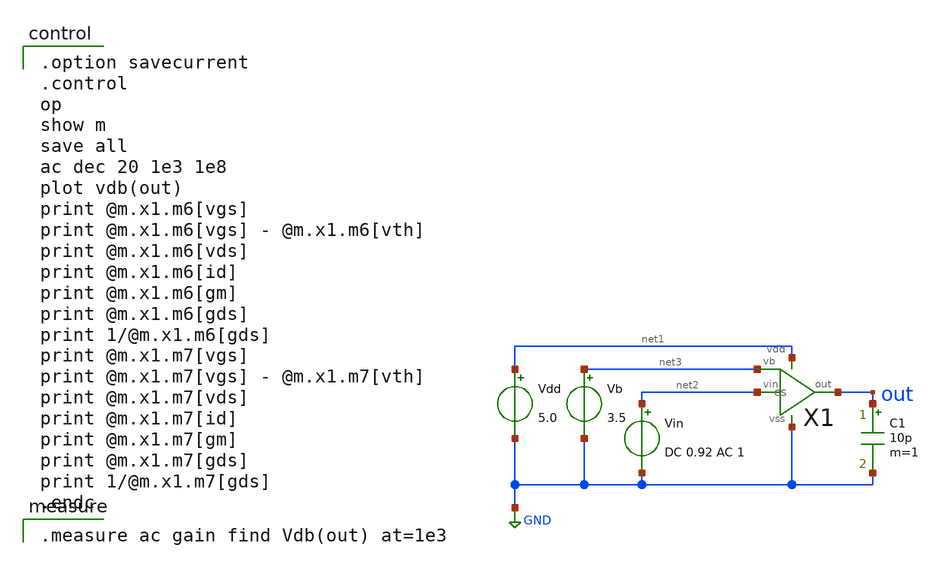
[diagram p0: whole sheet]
** sch_path: OR1/PTC06/opamp/cs_ac.sch
**.subckt cs_ac
Vdd net1 GND 5.0
Vb net3 GND 3.5
Vin net2 GND DC 0.92 AC 1
X1 net2 net3 out net1 GND cs
C1 out GND 10p m=1
**** begin user architecture code

.option savecurrent
.control
op
show m
save all
ac dec 20 1e3 1e8
plot vdb(out)
print @m.x1.m6[vgs]
print @m.x1.m6[vgs] - @m.x1.m6[vth]
print @m.x1.m6[vds]
print @m.x1.m6[id]
print @m.x1.m6[gm]
print @m.x1.m6[gds]
print 1/@m.x1.m6[gds]
print @m.x1.m7[vgs]
print @m.x1.m7[vgs] - @m.x1.m7[vth]
print @m.x1.m7[vds]
print @m.x1.m7[id]
print @m.x1.m7[gm]
print @m.x1.m7[gds]
print 1/@m.x1.m7[gds]
.endc


.measure ac gain find Vdb(out) at=1e3

 .include $::LIB/mos.lib
.include $::LIB/passive.lib
.include $::LIB/diode.lib
**** end user architecture code
**.ends

* expanding   symbol:  cs.sym # of pins=5
** sym_path: cs.sym
** sch_path: cs.sch
.subckt cs vin vb out vdd vss
*.ipin vb
*.ipin vin
*.opin out
*.iopin vss
*.iopin vdd
M6 out vb vdd vdd pmos L=2u W=400u m=1
M7 out vin vss vss nmos L=2u W=200u m=1
.ends

.GLOBAL GND
.end
